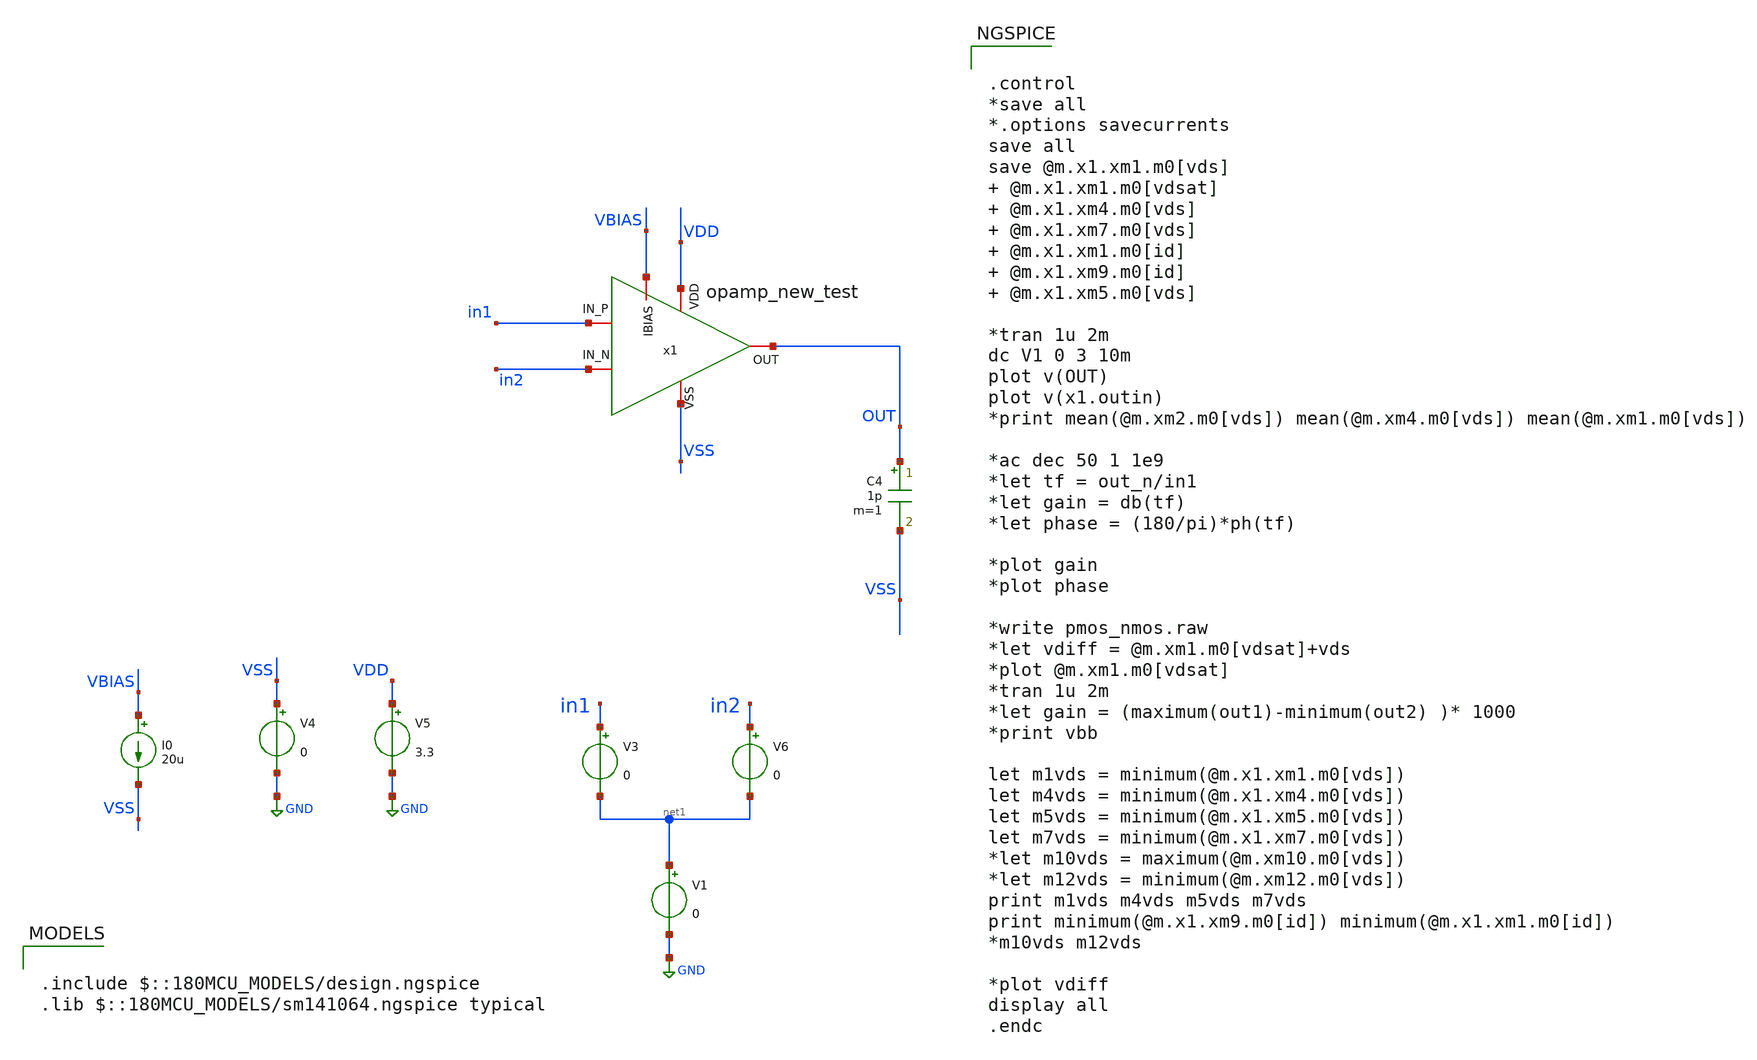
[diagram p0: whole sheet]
** sch_path: SCOP_INPUT_AND_MUX_PAKISTAN_03/Xschem/Folded_single/OTA_two_stage_trans.sch
**.subckt OTA_two_stage_trans
V3 in1 net1 0
V4 VSS GND 0
V5 VDD GND 3.3
V6 in2 net1 0
V1 net1 GND 0
C4 OUT VSS 1p m=1
I0 VBIAS VSS 20u
x1 OUT VDD VSS in2 in1 VBIAS opamp_new_test
**** begin user architecture code

.include $::180MCU_MODELS/design.ngspice
.lib $::180MCU_MODELS/sm141064.ngspice typical



.control
*save all
*.options savecurrents
save all
save @m.x1.xm1.m0[vds]  @m.x1.xm1.m0[vdsat]  @m.x1.xm4.m0[vds]  @m.x1.xm7.m0[vds]  @m.x1.xm1.m0[id]
+  @m.x1.xm9.m0[id]  @m.x1.xm5.m0[vds]

*tran 1u 2m
dc V1 0 3 10m
plot v(OUT)
plot v(x1.outin)
*print mean(@m.xm2.m0[vds]) mean(@m.xm4.m0[vds]) mean(@m.xm1.m0[vds])

*ac dec 50 1 1e9
*let tf = out_n/in1
*let gain = db(tf)
*let phase = (180/pi)*ph(tf)

*plot gain
*plot phase

*write pmos_nmos.raw
*let vdiff = @m.xm1.m0[vdsat]+vds
*plot @m.xm1.m0[vdsat]
*tran 1u 2m
*let gain = (maximum(out1)-minimum(out2) )* 1000
*print vbb

let m1vds = minimum(@m.x1.xm1.m0[vds])
let m4vds = minimum(@m.x1.xm4.m0[vds])
let m5vds = minimum(@m.x1.xm5.m0[vds])
let m7vds = minimum(@m.x1.xm7.m0[vds])
*let m10vds = maximum(@m.xm10.m0[vds])
*let m12vds = minimum(@m.xm12.m0[vds])
print m1vds m4vds m5vds m7vds
print minimum(@m.x1.xm9.m0[id]) minimum(@m.x1.xm1.m0[id])
*m10vds m12vds

*plot vdiff
display all
.endc


**** end user architecture code
**.ends

* expanding   symbol:  opamp_new_test.sym # of pins=6
** sym_path: SCOP_INPUT_AND_MUX_PAKISTAN_03/Xschem/Folded_single/opamp_new_test.sym
** sch_path: SCOP_INPUT_AND_MUX_PAKISTAN_03/Xschem/Folded_single/opamp_new_test.sch
.subckt opamp_new_test OUT VDD VSS IN_N IN_P IBIAS
*.iopin VDD
*.iopin VSS
*.iopin IN_N
*.iopin IN_P
*.iopin OUT
*.iopin IBIAS
XM15 IBIAS IBIAS VDD VDD pfet_03v3 L=0.56u W=4u nf=1 ad='int((nf+1)/2) * W/nf * 0.18u' as='int((nf+2)/2) * W/nf * 0.18u'
+ pd='2*int((nf+1)/2) * (W/nf + 0.18u)' ps='2*int((nf+2)/2) * (W/nf + 0.18u)' nrd='0.18u / W' nrs='0.18u / W'
+ sa=0 sb=0 sd=0 m=1
XM16 VB3 IBIAS VDD VDD pfet_03v3 L=0.56u W=4u nf=1 ad='int((nf+1)/2) * W/nf * 0.18u' as='int((nf+2)/2) * W/nf * 0.18u'
+ pd='2*int((nf+1)/2) * (W/nf + 0.18u)' ps='2*int((nf+2)/2) * (W/nf + 0.18u)' nrd='0.18u / W' nrs='0.18u / W'
+ sa=0 sb=0 sd=0 m=1
XM17 VB3 VB3 VSS VSS nfet_03v3 L=0.56u W=2u nf=1 ad='int((nf+1)/2) * W/nf * 0.18u' as='int((nf+2)/2) * W/nf * 0.18u'
+ pd='2*int((nf+1)/2) * (W/nf + 0.18u)' ps='2*int((nf+2)/2) * (W/nf + 0.18u)' nrd='0.18u / W' nrs='0.18u / W'
+ sa=0 sb=0 sd=0 m=1
XM19 VBIASN IBIAS VDD VDD pfet_03v3 L=0.56u W=4u nf=1 ad='int((nf+1)/2) * W/nf * 0.18u' as='int((nf+2)/2) * W/nf * 0.18u'
+ pd='2*int((nf+1)/2) * (W/nf + 0.18u)' ps='2*int((nf+2)/2) * (W/nf + 0.18u)' nrd='0.18u / W' nrs='0.18u / W'
+ sa=0 sb=0 sd=0 m=1
XM20 VBIASN VBIASN VSS VSS nfet_03v3 L=0.56u W=2u nf=1 ad='int((nf+1)/2) * W/nf * 0.18u' as='int((nf+2)/2) * W/nf * 0.18u'
+ pd='2*int((nf+1)/2) * (W/nf + 0.18u)' ps='2*int((nf+2)/2) * (W/nf + 0.18u)' nrd='0.18u / W' nrs='0.18u / W'
+ sa=0 sb=0 sd=0 m=1
XM26 VB2 VB2 VDD VDD pfet_03v3 L=0.56u W=900n nf=1 ad='int((nf+1)/2) * W/nf * 0.18u' as='int((nf+2)/2) * W/nf * 0.18u'
+ pd='2*int((nf+1)/2) * (W/nf + 0.18u)' ps='2*int((nf+2)/2) * (W/nf + 0.18u)' nrd='0.18u / W' nrs='0.18u / W'
+ sa=0 sb=0 sd=0 m=1
XM28 VB2 VBIASN VSS VSS nfet_03v3 L=0.56u W=2u nf=1 ad='int((nf+1)/2) * W/nf * 0.18u' as='int((nf+2)/2) * W/nf * 0.18u'
+ pd='2*int((nf+1)/2) * (W/nf + 0.18u)' ps='2*int((nf+2)/2) * (W/nf + 0.18u)' nrd='0.18u / W' nrs='0.18u / W'
+ sa=0 sb=0 sd=0 m=1
XM29 IBIAS2 IBIAS2 VDD VDD pfet_03v3 L=0.28u W=2u nf=1 ad='int((nf+1)/2) * W/nf * 0.18u' as='int((nf+2)/2) * W/nf * 0.18u'
+ pd='2*int((nf+1)/2) * (W/nf + 0.18u)' ps='2*int((nf+2)/2) * (W/nf + 0.18u)' nrd='0.18u / W' nrs='0.18u / W'
+ sa=0 sb=0 sd=0 m=1
XM30 IBIAS2 VBIASN VSS VSS nfet_03v3 L=0.56u W=2u nf=1 ad='int((nf+1)/2) * W/nf * 0.18u' as='int((nf+2)/2) * W/nf * 0.18u'
+ pd='2*int((nf+1)/2) * (W/nf + 0.18u)' ps='2*int((nf+2)/2) * (W/nf + 0.18u)' nrd='0.18u / W' nrs='0.18u / W'
+ sa=0 sb=0 sd=0 m=1
XM32 OUT IBIAS2 VDD VDD pfet_03v3 L=0.28u W=65u nf=1 ad='int((nf+1)/2) * W/nf * 0.18u' as='int((nf+2)/2) * W/nf * 0.18u'
+ pd='2*int((nf+1)/2) * (W/nf + 0.18u)' ps='2*int((nf+2)/2) * (W/nf + 0.18u)' nrd='0.18u / W' nrs='0.18u / W'
+ sa=0 sb=0 sd=0 m=1
XM33 OUT OUTin VSS VSS nfet_03v3 L=0.28u W=85u nf=1 ad='int((nf+1)/2) * W/nf * 0.18u' as='int((nf+2)/2) * W/nf * 0.18u'
+ pd='2*int((nf+1)/2) * (W/nf + 0.18u)' ps='2*int((nf+2)/2) * (W/nf + 0.18u)' nrd='0.18u / W' nrs='0.18u / W'
+ sa=0 sb=0 sd=0 m=1
R6 net1 OUTin 700 m=1
XM41 OUT OUTin VSS VSS nfet_03v3 L=0.28u W=85u nf=1 ad='int((nf+1)/2) * W/nf * 0.18u' as='int((nf+2)/2) * W/nf * 0.18u'
+ pd='2*int((nf+1)/2) * (W/nf + 0.18u)' ps='2*int((nf+2)/2) * (W/nf + 0.18u)' nrd='0.18u / W' nrs='0.18u / W'
+ sa=0 sb=0 sd=0 m=1
XM12 VB4 VB4 VSS VSS nfet_03v3 L=0.28u W=7u nf=1 ad='int((nf+1)/2) * W/nf * 0.18u' as='int((nf+2)/2) * W/nf * 0.18u'
+ pd='2*int((nf+1)/2) * (W/nf + 0.18u)' ps='2*int((nf+2)/2) * (W/nf + 0.18u)' nrd='0.18u / W' nrs='0.18u / W'
+ sa=0 sb=0 sd=0 m=1
XM13 net2 net2 VB4 VSS nfet_03v3 L=0.56u W=1u nf=1 ad='int((nf+1)/2) * W/nf * 0.18u' as='int((nf+2)/2) * W/nf * 0.18u'
+ pd='2*int((nf+1)/2) * (W/nf + 0.18u)' ps='2*int((nf+2)/2) * (W/nf + 0.18u)' nrd='0.18u / W' nrs='0.18u / W'
+ sa=0 sb=0 sd=0 m=1
XM14 net2 IBIAS VDD VDD pfet_03v3 L=0.56u W=4u nf=1 ad='int((nf+1)/2) * W/nf * 0.18u' as='int((nf+2)/2) * W/nf * 0.18u'
+ pd='2*int((nf+1)/2) * (W/nf + 0.18u)' ps='2*int((nf+2)/2) * (W/nf + 0.18u)' nrd='0.18u / W' nrs='0.18u / W'
+ sa=0 sb=0 sd=0 m=1
XM21 OUT IBIAS2 VDD VDD pfet_03v3 L=0.28u W=65u nf=1 ad='int((nf+1)/2) * W/nf * 0.18u' as='int((nf+2)/2) * W/nf * 0.18u'
+ pd='2*int((nf+1)/2) * (W/nf + 0.18u)' ps='2*int((nf+2)/2) * (W/nf + 0.18u)' nrd='0.18u / W' nrs='0.18u / W'
+ sa=0 sb=0 sd=0 m=1
C1 net1 OUT 0.7p m=1
x1 net3 net4 net5 IN_N IN_P net6 folded_single
.ends


* expanding   symbol:  folded_single.sym # of pins=6
** sym_path: AWG_OUTPUT_AND_MUX_PAKISTAN_05/xschem/folded_single.sym
** sch_path: AWG_OUTPUT_AND_MUX_PAKISTAN_05/xschem/folded_single.sch
.subckt folded_single OUTo VDD VSS VINN VINP IBIAS
*.iopin VDD
*.iopin VSS
*.iopin VINN
*.iopin VINP
*.iopin IBIAS
*.iopin OUTo
XM1 net1 IBIAS VDD VDD pfet_03v3 L=0.56u W=24u nf=1 ad='int((nf+1)/2) * W/nf * 0.18u' as='int((nf+2)/2) * W/nf * 0.18u'
+ pd='2*int((nf+1)/2) * (W/nf + 0.18u)' ps='2*int((nf+2)/2) * (W/nf + 0.18u)' nrd='0.18u / W' nrs='0.18u / W'
+ sa=0 sb=0 sd=0 m=1
XM2 net2 IBIAS VDD VDD pfet_03v3 L=0.56u W=24u nf=1 ad='int((nf+1)/2) * W/nf * 0.18u' as='int((nf+2)/2) * W/nf * 0.18u'
+ pd='2*int((nf+1)/2) * (W/nf + 0.18u)' ps='2*int((nf+2)/2) * (W/nf + 0.18u)' nrd='0.18u / W' nrs='0.18u / W'
+ sa=0 sb=0 sd=0 m=1
XM3 net3 VBS2 net2 VDD pfet_03v3 L=0.28u W=12u nf=1 ad='int((nf+1)/2) * W/nf * 0.18u' as='int((nf+2)/2) * W/nf * 0.18u'
+ pd='2*int((nf+1)/2) * (W/nf + 0.18u)' ps='2*int((nf+2)/2) * (W/nf + 0.18u)' nrd='0.18u / W' nrs='0.18u / W'
+ sa=0 sb=0 sd=0 m=1
XM4 OUT VBS2 net1 VDD pfet_03v3 L=0.28u W=12u nf=1 ad='int((nf+1)/2) * W/nf * 0.18u' as='int((nf+2)/2) * W/nf * 0.18u'
+ pd='2*int((nf+1)/2) * (W/nf + 0.18u)' ps='2*int((nf+2)/2) * (W/nf + 0.18u)' nrd='0.18u / W' nrs='0.18u / W'
+ sa=0 sb=0 sd=0 m=1
XM5 OUT VBS3 net5 VSS nfet_03v3 L=0.28u W=24u nf=1 ad='int((nf+1)/2) * W/nf * 0.18u' as='int((nf+2)/2) * W/nf * 0.18u'
+ pd='2*int((nf+1)/2) * (W/nf + 0.18u)' ps='2*int((nf+2)/2) * (W/nf + 0.18u)' nrd='0.18u / W' nrs='0.18u / W'
+ sa=0 sb=0 sd=0 m=1
XM6 net3 VBS3 net4 VSS nfet_03v3 L=0.28u W=24u nf=1 ad='int((nf+1)/2) * W/nf * 0.18u' as='int((nf+2)/2) * W/nf * 0.18u'
+ pd='2*int((nf+1)/2) * (W/nf + 0.18u)' ps='2*int((nf+2)/2) * (W/nf + 0.18u)' nrd='0.18u / W' nrs='0.18u / W'
+ sa=0 sb=0 sd=0 m=1
XM7 net5 net3 VSS VSS nfet_03v3 L=0.28u W=48u nf=1 ad='int((nf+1)/2) * W/nf * 0.18u' as='int((nf+2)/2) * W/nf * 0.18u'
+ pd='2*int((nf+1)/2) * (W/nf + 0.18u)' ps='2*int((nf+2)/2) * (W/nf + 0.18u)' nrd='0.18u / W' nrs='0.18u / W'
+ sa=0 sb=0 sd=0 m=1
XM8 net4 net3 VSS VSS nfet_03v3 L=0.28u W=48u nf=1 ad='int((nf+1)/2) * W/nf * 0.18u' as='int((nf+2)/2) * W/nf * 0.18u'
+ pd='2*int((nf+1)/2) * (W/nf + 0.18u)' ps='2*int((nf+2)/2) * (W/nf + 0.18u)' nrd='0.18u / W' nrs='0.18u / W'
+ sa=0 sb=0 sd=0 m=1
XM9 net6 IBIAS VDD VDD pfet_03v3 L=0.56u W=48u nf=1 ad='int((nf+1)/2) * W/nf * 0.18u' as='int((nf+2)/2) * W/nf * 0.18u'
+ pd='2*int((nf+1)/2) * (W/nf + 0.18u)' ps='2*int((nf+2)/2) * (W/nf + 0.18u)' nrd='0.18u / W' nrs='0.18u / W'
+ sa=0 sb=0 sd=0 m=1
XM10 net5 VINP net6 VDD pfet_03v3 L=0.28u W=48u nf=1 ad='int((nf+1)/2) * W/nf * 0.18u' as='int((nf+2)/2) * W/nf * 0.18u'
+ pd='2*int((nf+1)/2) * (W/nf + 0.18u)' ps='2*int((nf+2)/2) * (W/nf + 0.18u)' nrd='0.18u / W' nrs='0.18u / W'
+ sa=0 sb=0 sd=0 m=1
XM11 net4 VINN net6 VDD pfet_03v3 L=0.28u W=48u nf=1 ad='int((nf+1)/2) * W/nf * 0.18u' as='int((nf+2)/2) * W/nf * 0.18u'
+ pd='2*int((nf+1)/2) * (W/nf + 0.18u)' ps='2*int((nf+2)/2) * (W/nf + 0.18u)' nrd='0.18u / W' nrs='0.18u / W'
+ sa=0 sb=0 sd=0 m=1
XM12 net1 net1 net1 VDD pfet_03v3 L=0.56u W=12u nf=1 ad='int((nf+1)/2) * W/nf * 0.18u' as='int((nf+2)/2) * W/nf * 0.18u'
+ pd='2*int((nf+1)/2) * (W/nf + 0.18u)' ps='2*int((nf+2)/2) * (W/nf + 0.18u)' nrd='0.18u / W' nrs='0.18u / W'
+ sa=0 sb=0 sd=0 m=1
XM13 net2 net2 net2 VDD pfet_03v3 L=0.56u W=12u nf=1 ad='int((nf+1)/2) * W/nf * 0.18u' as='int((nf+2)/2) * W/nf * 0.18u'
+ pd='2*int((nf+1)/2) * (W/nf + 0.18u)' ps='2*int((nf+2)/2) * (W/nf + 0.18u)' nrd='0.18u / W' nrs='0.18u / W'
+ sa=0 sb=0 sd=0 m=1
XM15 OUT OUT OUT VDD pfet_03v3 L=0.28u W=12u nf=1 ad='int((nf+1)/2) * W/nf * 0.18u' as='int((nf+2)/2) * W/nf * 0.18u'
+ pd='2*int((nf+1)/2) * (W/nf + 0.18u)' ps='2*int((nf+2)/2) * (W/nf + 0.18u)' nrd='0.18u / W' nrs='0.18u / W'
+ sa=0 sb=0 sd=0 m=1
XM18 net6 net6 net6 VDD pfet_03v3 L=0.56u W=24u nf=1 ad='int((nf+1)/2) * W/nf * 0.18u' as='int((nf+2)/2) * W/nf * 0.18u'
+ pd='2*int((nf+1)/2) * (W/nf + 0.18u)' ps='2*int((nf+2)/2) * (W/nf + 0.18u)' nrd='0.18u / W' nrs='0.18u / W'
+ sa=0 sb=0 sd=0 m=1
XM14 OUT OUT OUT VSS nfet_03v3 L=0.28u W=12u nf=1 ad='int((nf+1)/2) * W/nf * 0.18u' as='int((nf+2)/2) * W/nf * 0.18u'
+ pd='2*int((nf+1)/2) * (W/nf + 0.18u)' ps='2*int((nf+2)/2) * (W/nf + 0.18u)' nrd='0.18u / W' nrs='0.18u / W'
+ sa=0 sb=0 sd=0 m=1
XM16 net3 net3 net3 VSS nfet_03v3 L=0.28u W=12u nf=1 ad='int((nf+1)/2) * W/nf * 0.18u' as='int((nf+2)/2) * W/nf * 0.18u'
+ pd='2*int((nf+1)/2) * (W/nf + 0.18u)' ps='2*int((nf+2)/2) * (W/nf + 0.18u)' nrd='0.18u / W' nrs='0.18u / W'
+ sa=0 sb=0 sd=0 m=1
XM17 net4 net4 net4 VSS nfet_03v3 L=0.28u W=12u nf=1 ad='int((nf+1)/2) * W/nf * 0.18u' as='int((nf+2)/2) * W/nf * 0.18u'
+ pd='2*int((nf+1)/2) * (W/nf + 0.18u)' ps='2*int((nf+2)/2) * (W/nf + 0.18u)' nrd='0.18u / W' nrs='0.18u / W'
+ sa=0 sb=0 sd=0 m=1
XM19 net5 net5 net5 VSS nfet_03v3 L=0.28u W=12u nf=1 ad='int((nf+1)/2) * W/nf * 0.18u' as='int((nf+2)/2) * W/nf * 0.18u'
+ pd='2*int((nf+1)/2) * (W/nf + 0.18u)' ps='2*int((nf+2)/2) * (W/nf + 0.18u)' nrd='0.18u / W' nrs='0.18u / W'
+ sa=0 sb=0 sd=0 m=1
XM20 net4 net4 net4 VDD pfet_03v3 L=0.28u W=12u nf=1 ad='int((nf+1)/2) * W/nf * 0.18u' as='int((nf+2)/2) * W/nf * 0.18u'
+ pd='2*int((nf+1)/2) * (W/nf + 0.18u)' ps='2*int((nf+2)/2) * (W/nf + 0.18u)' nrd='0.18u / W' nrs='0.18u / W'
+ sa=0 sb=0 sd=0 m=1
XM21 net5 net5 net5 VDD pfet_03v3 L=0.28u W=12u nf=1 ad='int((nf+1)/2) * W/nf * 0.18u' as='int((nf+2)/2) * W/nf * 0.18u'
+ pd='2*int((nf+1)/2) * (W/nf + 0.18u)' ps='2*int((nf+2)/2) * (W/nf + 0.18u)' nrd='0.18u / W' nrs='0.18u / W'
+ sa=0 sb=0 sd=0 m=1
XM22 VBS3 IBIAS VDD VDD pfet_03v3 L=0.56u W=8u nf=1 ad='int((nf+1)/2) * W/nf * 0.18u' as='int((nf+2)/2) * W/nf * 0.18u'
+ pd='2*int((nf+1)/2) * (W/nf + 0.18u)' ps='2*int((nf+2)/2) * (W/nf + 0.18u)' nrd='0.18u / W' nrs='0.18u / W'
+ sa=0 sb=0 sd=0 m=1
XM23 VBS3 VBS3 VSS VSS nfet_03v3 L=0.56u W=4u nf=1 ad='int((nf+1)/2) * W/nf * 0.18u' as='int((nf+2)/2) * W/nf * 0.18u'
+ pd='2*int((nf+1)/2) * (W/nf + 0.18u)' ps='2*int((nf+2)/2) * (W/nf + 0.18u)' nrd='0.18u / W' nrs='0.18u / W'
+ sa=0 sb=0 sd=0 m=1
XM24 VBIASN IBIAS VDD VDD pfet_03v3 L=0.56u W=4u nf=1 ad='int((nf+1)/2) * W/nf * 0.18u' as='int((nf+2)/2) * W/nf * 0.18u'
+ pd='2*int((nf+1)/2) * (W/nf + 0.18u)' ps='2*int((nf+2)/2) * (W/nf + 0.18u)' nrd='0.18u / W' nrs='0.18u / W'
+ sa=0 sb=0 sd=0 m=1
XM25 VBIASN VBIASN VSS VSS nfet_03v3 L=0.56u W=2u nf=1 ad='int((nf+1)/2) * W/nf * 0.18u' as='int((nf+2)/2) * W/nf * 0.18u'
+ pd='2*int((nf+1)/2) * (W/nf + 0.18u)' ps='2*int((nf+2)/2) * (W/nf + 0.18u)' nrd='0.18u / W' nrs='0.18u / W'
+ sa=0 sb=0 sd=0 m=1
XM26 IBIAS IBIAS VDD VDD pfet_03v3 L=0.56u W=6u nf=1 ad='int((nf+1)/2) * W/nf * 0.18u' as='int((nf+2)/2) * W/nf * 0.18u'
+ pd='2*int((nf+1)/2) * (W/nf + 0.18u)' ps='2*int((nf+2)/2) * (W/nf + 0.18u)' nrd='0.18u / W' nrs='0.18u / W'
+ sa=0 sb=0 sd=0 m=1
XM27 VBS2 VBS2 VDD VDD pfet_03v3 L=0.56u W=2u nf=1 ad='int((nf+1)/2) * W/nf * 0.18u' as='int((nf+2)/2) * W/nf * 0.18u'
+ pd='2*int((nf+1)/2) * (W/nf + 0.18u)' ps='2*int((nf+2)/2) * (W/nf + 0.18u)' nrd='0.18u / W' nrs='0.18u / W'
+ sa=0 sb=0 sd=0 m=1
XM28 VBS2 VBIASN VSS VSS nfet_03v3 L=0.56u W=4u nf=1 ad='int((nf+1)/2) * W/nf * 0.18u' as='int((nf+2)/2) * W/nf * 0.18u'
+ pd='2*int((nf+1)/2) * (W/nf + 0.18u)' ps='2*int((nf+2)/2) * (W/nf + 0.18u)' nrd='0.18u / W' nrs='0.18u / W'
+ sa=0 sb=0 sd=0 m=1
XM29 VDD VDD VDD VDD pfet_03v3 L=0.56u W=8u nf=1 ad='int((nf+1)/2) * W/nf * 0.18u' as='int((nf+2)/2) * W/nf * 0.18u'
+ pd='2*int((nf+1)/2) * (W/nf + 0.18u)' ps='2*int((nf+2)/2) * (W/nf + 0.18u)' nrd='0.18u / W' nrs='0.18u / W'
+ sa=0 sb=0 sd=0 m=1
XM31 net4 net4 VSS VSS nfet_03v3 L=0.28u W=18u nf=1 ad='int((nf+1)/2) * W/nf * 0.18u' as='int((nf+2)/2) * W/nf * 0.18u'
+ pd='2*int((nf+1)/2) * (W/nf + 0.18u)' ps='2*int((nf+2)/2) * (W/nf + 0.18u)' nrd='0.18u / W' nrs='0.18u / W'
+ sa=0 sb=0 sd=0 m=1
XM32 net5 net5 VSS VSS nfet_03v3 L=0.28u W=18u nf=1 ad='int((nf+1)/2) * W/nf * 0.18u' as='int((nf+2)/2) * W/nf * 0.18u'
+ pd='2*int((nf+1)/2) * (W/nf + 0.18u)' ps='2*int((nf+2)/2) * (W/nf + 0.18u)' nrd='0.18u / W' nrs='0.18u / W'
+ sa=0 sb=0 sd=0 m=1
XM33 IBIAS2 IBIAS2 VDD VDD pfet_03v3 L=1u W=4u nf=1 ad='int((nf+1)/2) * W/nf * 0.18u' as='int((nf+2)/2) * W/nf * 0.18u'
+ pd='2*int((nf+1)/2) * (W/nf + 0.18u)' ps='2*int((nf+2)/2) * (W/nf + 0.18u)' nrd='0.18u / W' nrs='0.18u / W'
+ sa=0 sb=0 sd=0 m=1
XM34 IBIAS2 VBIASN VSS VSS nfet_03v3 L=0.56u W=2u nf=1 ad='int((nf+1)/2) * W/nf * 0.18u' as='int((nf+2)/2) * W/nf * 0.18u'
+ pd='2*int((nf+1)/2) * (W/nf + 0.18u)' ps='2*int((nf+2)/2) * (W/nf + 0.18u)' nrd='0.18u / W' nrs='0.18u / W'
+ sa=0 sb=0 sd=0 m=1
XM35 VBIASN2 IBIAS2 VDD VDD pfet_03v3 L=1u W=16u nf=1 ad='int((nf+1)/2) * W/nf * 0.18u' as='int((nf+2)/2) * W/nf * 0.18u'
+ pd='2*int((nf+1)/2) * (W/nf + 0.18u)' ps='2*int((nf+2)/2) * (W/nf + 0.18u)' nrd='0.18u / W' nrs='0.18u / W'
+ sa=0 sb=0 sd=0 m=1
XM36 VBIASN2 VBIASN2 VSS VSS nfet_03v3 L=1u W=12u nf=1 ad='int((nf+1)/2) * W/nf * 0.18u' as='int((nf+2)/2) * W/nf * 0.18u'
+ pd='2*int((nf+1)/2) * (W/nf + 0.18u)' ps='2*int((nf+2)/2) * (W/nf + 0.18u)' nrd='0.18u / W' nrs='0.18u / W'
+ sa=0 sb=0 sd=0 m=1
XM37 IBIAS3 VBIASN2 VSS VSS nfet_03v3 L=1u W=36u nf=1 ad='int((nf+1)/2) * W/nf * 0.18u' as='int((nf+2)/2) * W/nf * 0.18u'
+ pd='2*int((nf+1)/2) * (W/nf + 0.18u)' ps='2*int((nf+2)/2) * (W/nf + 0.18u)' nrd='0.18u / W' nrs='0.18u / W'
+ sa=0 sb=0 sd=0 m=1
XM38 IBIAS3 IBIAS3 VDD VDD pfet_03v3 L=0.28u W=90u nf=1 ad='int((nf+1)/2) * W/nf * 0.18u' as='int((nf+2)/2) * W/nf * 0.18u'
+ pd='2*int((nf+1)/2) * (W/nf + 0.18u)' ps='2*int((nf+2)/2) * (W/nf + 0.18u)' nrd='0.18u / W' nrs='0.18u / W'
+ sa=0 sb=0 sd=0 m=1
XM39 OUTo IBIAS3 VDD VDD pfet_03v3 L=0.28u W=90u nf=1 ad='int((nf+1)/2) * W/nf * 0.18u' as='int((nf+2)/2) * W/nf * 0.18u'
+ pd='2*int((nf+1)/2) * (W/nf + 0.18u)' ps='2*int((nf+2)/2) * (W/nf + 0.18u)' nrd='0.18u / W' nrs='0.18u / W'
+ sa=0 sb=0 sd=0 m=1
XM40 OUTo IBIAS3 VDD VDD pfet_03v3 L=0.28u W=90u nf=1 ad='int((nf+1)/2) * W/nf * 0.18u' as='int((nf+2)/2) * W/nf * 0.18u'
+ pd='2*int((nf+1)/2) * (W/nf + 0.18u)' ps='2*int((nf+2)/2) * (W/nf + 0.18u)' nrd='0.18u / W' nrs='0.18u / W'
+ sa=0 sb=0 sd=0 m=1
XM41 OUTo IBIAS3 VDD VDD pfet_03v3 L=0.28u W=90u nf=1 ad='int((nf+1)/2) * W/nf * 0.18u' as='int((nf+2)/2) * W/nf * 0.18u'
+ pd='2*int((nf+1)/2) * (W/nf + 0.18u)' ps='2*int((nf+2)/2) * (W/nf + 0.18u)' nrd='0.18u / W' nrs='0.18u / W'
+ sa=0 sb=0 sd=0 m=1
XM42 OUTo IBIAS3 VDD VDD pfet_03v3 L=0.28u W=90u nf=1 ad='int((nf+1)/2) * W/nf * 0.18u' as='int((nf+2)/2) * W/nf * 0.18u'
+ pd='2*int((nf+1)/2) * (W/nf + 0.18u)' ps='2*int((nf+2)/2) * (W/nf + 0.18u)' nrd='0.18u / W' nrs='0.18u / W'
+ sa=0 sb=0 sd=0 m=1
XM43 VDD VDD VDD VDD pfet_03v3 L=1u W=8u nf=1 ad='int((nf+1)/2) * W/nf * 0.18u' as='int((nf+2)/2) * W/nf * 0.18u'
+ pd='2*int((nf+1)/2) * (W/nf + 0.18u)' ps='2*int((nf+2)/2) * (W/nf + 0.18u)' nrd='0.18u / W' nrs='0.18u / W'
+ sa=0 sb=0 sd=0 m=1
XM45 VDD VDD VDD VDD pfet_03v3 L=0.28u W=90u nf=1 ad='int((nf+1)/2) * W/nf * 0.18u' as='int((nf+2)/2) * W/nf * 0.18u'
+ pd='2*int((nf+1)/2) * (W/nf + 0.18u)' ps='2*int((nf+2)/2) * (W/nf + 0.18u)' nrd='0.18u / W' nrs='0.18u / W'
+ sa=0 sb=0 sd=0 m=1
XM46 OUTo OUT VSS VSS nfet_03v3 L=0.28u W=90u nf=1 ad='int((nf+1)/2) * W/nf * 0.18u' as='int((nf+2)/2) * W/nf * 0.18u'
+ pd='2*int((nf+1)/2) * (W/nf + 0.18u)' ps='2*int((nf+2)/2) * (W/nf + 0.18u)' nrd='0.18u / W' nrs='0.18u / W'
+ sa=0 sb=0 sd=0 m=1
XM47 OUTo OUT VSS VSS nfet_03v3 L=0.28u W=90u nf=1 ad='int((nf+1)/2) * W/nf * 0.18u' as='int((nf+2)/2) * W/nf * 0.18u'
+ pd='2*int((nf+1)/2) * (W/nf + 0.18u)' ps='2*int((nf+2)/2) * (W/nf + 0.18u)' nrd='0.18u / W' nrs='0.18u / W'
+ sa=0 sb=0 sd=0 m=1
XR1 net7 OUTo VDD ppolyf_u r_width=0.8e-6 r_length=6.459e-6 m=1
XC1 net7 OUT cap_mim_2f0_m4m5_noshield c_width=24e-6 c_length=15.5e-6 m=2
XR2 net7 OUTo VDD ppolyf_u r_width=0.8e-6 r_length=6.459e-6 m=1
XR3 net7 OUTo VDD ppolyf_u r_width=0.8e-6 r_length=6.459e-6 m=1
XR4 net7 OUTo VDD ppolyf_u r_width=0.8e-6 r_length=6.459e-6 m=1
XR5 VDD VDD VDD ppolyf_u r_width=0.8e-6 r_length=6.459e-6 m=2
.ends

.GLOBAL GND
.end
